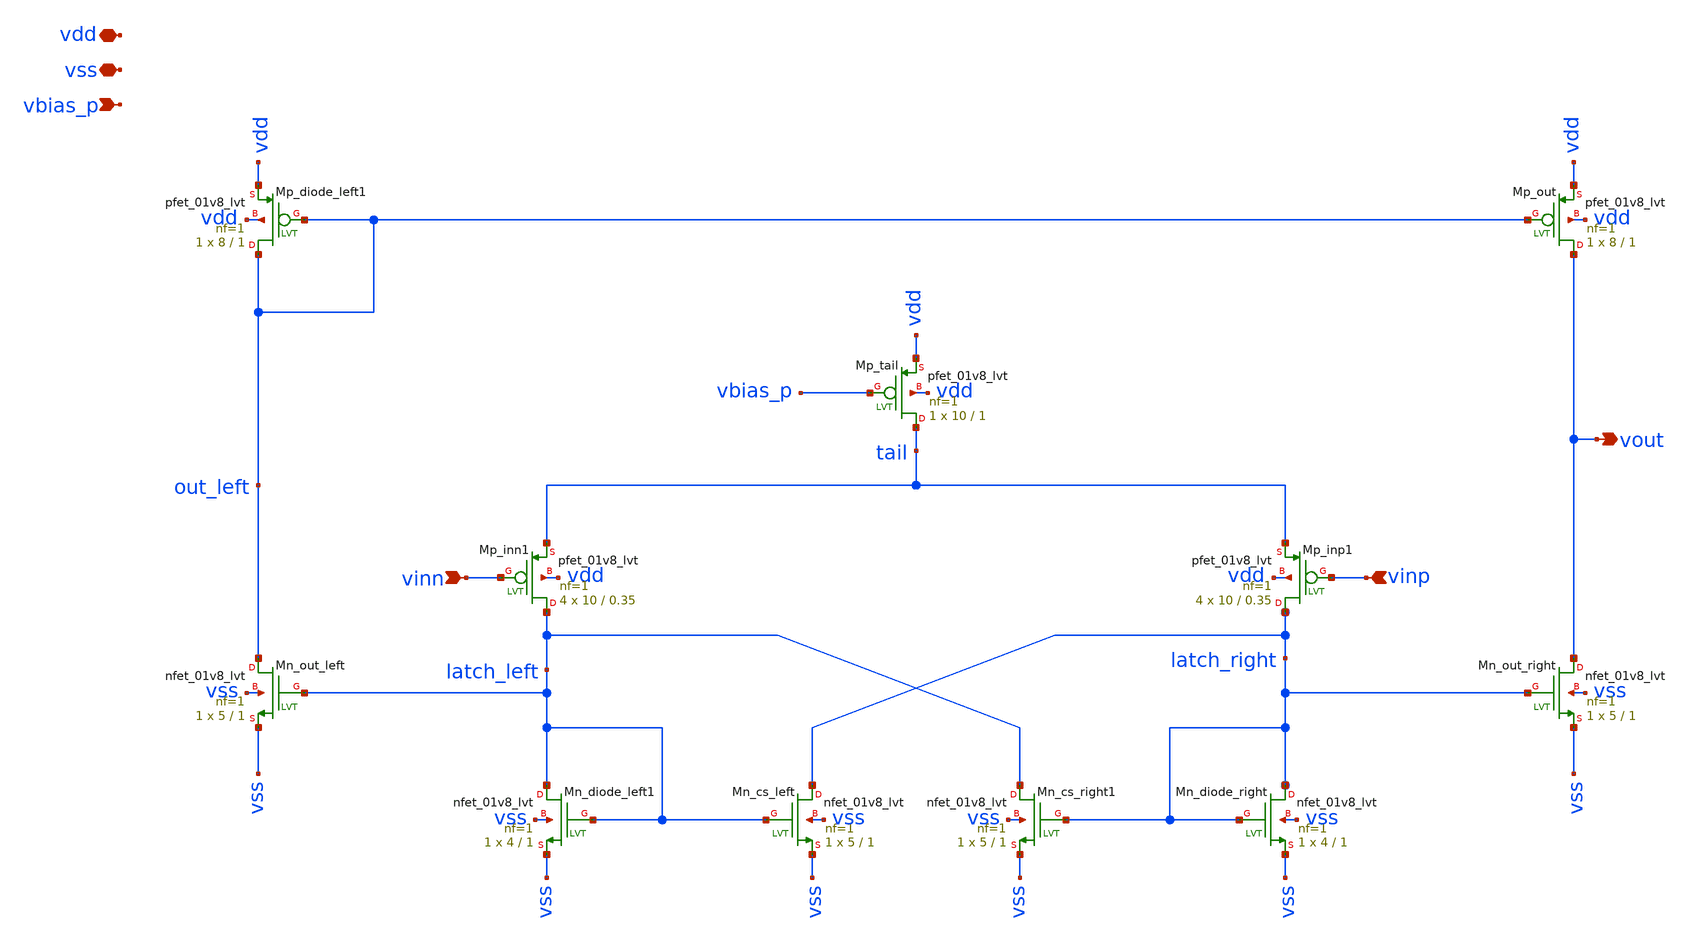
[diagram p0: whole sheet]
** sch_path: xsch/ip/comparators/comp_p/comp_p.sch
**.subckt comp_p vdd vss vbias_p vinn vinp vout
*.iopin vdd
*.iopin vss
*.ipin vbias_p
*.ipin vinn
*.ipin vinp
*.opin vout
XMp_inn1 latch_left vinn tail vdd sky130_fd_pr__pfet_01v8_lvt L=0.35 W=10 nf=1 ad='int((nf+1)/2) * W/nf * 0.29'
+ as='int((nf+2)/2) * W/nf * 0.29' pd='2*int((nf+1)/2) * (W/nf + 0.29)' ps='2*int((nf+2)/2) * (W/nf + 0.29)'
+ nrd='0.29 / W' nrs='0.29 / W' sa=0 sb=0 sd=0 mult=4 m=4
XMp_inp1 latch_right vinp tail vdd sky130_fd_pr__pfet_01v8_lvt L=0.35 W=10 nf=1 ad='int((nf+1)/2) * W/nf * 0.29'
+ as='int((nf+2)/2) * W/nf * 0.29' pd='2*int((nf+1)/2) * (W/nf + 0.29)' ps='2*int((nf+2)/2) * (W/nf + 0.29)'
+ nrd='0.29 / W' nrs='0.29 / W' sa=0 sb=0 sd=0 mult=4 m=4
XMn_diode_left1 latch_left latch_left vss vss sky130_fd_pr__nfet_01v8_lvt L=1 W=4 nf=1 ad='int((nf+1)/2) * W/nf * 0.29'
+ as='int((nf+2)/2) * W/nf * 0.29' pd='2*int((nf+1)/2) * (W/nf + 0.29)' ps='2*int((nf+2)/2) * (W/nf + 0.29)'
+ nrd='0.29 / W' nrs='0.29 / W' sa=0 sb=0 sd=0 mult=1 m=1
XMn_cs_left latch_right latch_left vss vss sky130_fd_pr__nfet_01v8_lvt L=1 W=5 nf=1 ad='int((nf+1)/2) * W/nf * 0.29'
+ as='int((nf+2)/2) * W/nf * 0.29' pd='2*int((nf+1)/2) * (W/nf + 0.29)' ps='2*int((nf+2)/2) * (W/nf + 0.29)'
+ nrd='0.29 / W' nrs='0.29 / W' sa=0 sb=0 sd=0 mult=1 m=1
XMn_diode_right latch_right latch_right vss vss sky130_fd_pr__nfet_01v8_lvt L=1 W=4 nf=1 ad='int((nf+1)/2) * W/nf * 0.29'
+ as='int((nf+2)/2) * W/nf * 0.29' pd='2*int((nf+1)/2) * (W/nf + 0.29)' ps='2*int((nf+2)/2) * (W/nf + 0.29)'
+ nrd='0.29 / W' nrs='0.29 / W' sa=0 sb=0 sd=0 mult=1 m=1
XMn_cs_right1 latch_left latch_right vss vss sky130_fd_pr__nfet_01v8_lvt L=1 W=5 nf=1 ad='int((nf+1)/2) * W/nf * 0.29'
+ as='int((nf+2)/2) * W/nf * 0.29' pd='2*int((nf+1)/2) * (W/nf + 0.29)' ps='2*int((nf+2)/2) * (W/nf + 0.29)'
+ nrd='0.29 / W' nrs='0.29 / W' sa=0 sb=0 sd=0 mult=1 m=1
XMp_tail tail vbias_p vdd vdd sky130_fd_pr__pfet_01v8_lvt L=1 W=10 nf=1 ad='int((nf+1)/2) * W/nf * 0.29'
+ as='int((nf+2)/2) * W/nf * 0.29' pd='2*int((nf+1)/2) * (W/nf + 0.29)' ps='2*int((nf+2)/2) * (W/nf + 0.29)'
+ nrd='0.29 / W' nrs='0.29 / W' sa=0 sb=0 sd=0 mult=1 m=1
XMn_out_right vout latch_right vss vss sky130_fd_pr__nfet_01v8_lvt L=1 W=5 nf=1 ad='int((nf+1)/2) * W/nf * 0.29'
+ as='int((nf+2)/2) * W/nf * 0.29' pd='2*int((nf+1)/2) * (W/nf + 0.29)' ps='2*int((nf+2)/2) * (W/nf + 0.29)'
+ nrd='0.29 / W' nrs='0.29 / W' sa=0 sb=0 sd=0 mult=1 m=1
XMn_out_left out_left latch_left vss vss sky130_fd_pr__nfet_01v8_lvt L=1 W=5 nf=1 ad='int((nf+1)/2) * W/nf * 0.29'
+ as='int((nf+2)/2) * W/nf * 0.29' pd='2*int((nf+1)/2) * (W/nf + 0.29)' ps='2*int((nf+2)/2) * (W/nf + 0.29)'
+ nrd='0.29 / W' nrs='0.29 / W' sa=0 sb=0 sd=0 mult=1 m=1
XMp_diode_left1 out_left out_left vdd vdd sky130_fd_pr__pfet_01v8_lvt L=1 W=8 nf=1 ad='int((nf+1)/2) * W/nf * 0.29'
+ as='int((nf+2)/2) * W/nf * 0.29' pd='2*int((nf+1)/2) * (W/nf + 0.29)' ps='2*int((nf+2)/2) * (W/nf + 0.29)'
+ nrd='0.29 / W' nrs='0.29 / W' sa=0 sb=0 sd=0 mult=1 m=1
XMp_out vout out_left vdd vdd sky130_fd_pr__pfet_01v8_lvt L=1 W=8 nf=1 ad='int((nf+1)/2) * W/nf * 0.29'
+ as='int((nf+2)/2) * W/nf * 0.29' pd='2*int((nf+1)/2) * (W/nf + 0.29)' ps='2*int((nf+2)/2) * (W/nf + 0.29)'
+ nrd='0.29 / W' nrs='0.29 / W' sa=0 sb=0 sd=0 mult=1 m=1
**.ends
.end
